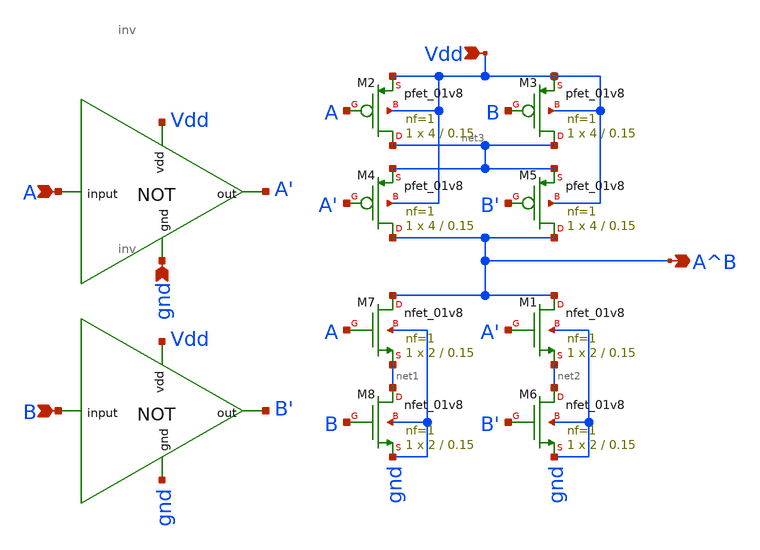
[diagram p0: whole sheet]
** sch_path: extra_stuff/xor.sch
**.subckt xor Vdd A B gnd A^B
*.ipin Vdd
*.ipin A
*.ipin B
*.ipin gnd
*.opin A^B
XM1 A^B A' net2 gnd sky130_fd_pr__nfet_01v8 L=0.15 W=2 nf=1 ad='int((1 + 1)/2) * 2 / 1 * 0.29' as='int((1
+ + 2)/2) * 2 / 1 * 0.29' pd='2*int((1 + 1)/2) * (2 / 1 + 0.29)' ps='2*int((1 + 2)/2) * (2 / 1 + 0.29)' nrd='0.29
+ / 2 ' nrs='0.29 / 2 ' sa=0 sb=0 sd=0 mult=1 m=1
XM2 net3 A Vdd Vdd sky130_fd_pr__pfet_01v8 L=0.15 W=4 nf=1 ad='int((1 + 1)/2) * 4 / 1 * 0.29' as='int((1
+ + 2)/2) * 4 / 1 * 0.29' pd='2*int((1 + 1)/2) * (4 / 1 + 0.29)' ps='2*int((1 + 2)/2) * (4 / 1 + 0.29)' nrd='0.29
+ / 4 ' nrs='0.29 / 4 ' sa=0 sb=0 sd=0 mult=1 m=1
XM3 net3 B Vdd Vdd sky130_fd_pr__pfet_01v8 L=0.15 W=4 nf=1 ad='int((1 + 1)/2) * 4 / 1 * 0.29' as='int((1
+ + 2)/2) * 4 / 1 * 0.29' pd='2*int((1 + 1)/2) * (4 / 1 + 0.29)' ps='2*int((1 + 2)/2) * (4 / 1 + 0.29)' nrd='0.29
+ / 4 ' nrs='0.29 / 4 ' sa=0 sb=0 sd=0 mult=1 m=1
XM4 A^B A' net3 Vdd sky130_fd_pr__pfet_01v8 L=0.15 W=4 nf=1 ad='int((1 + 1)/2) * 4 / 1 * 0.29' as='int((1 + 2)/2) * 4 / 1 * 0.29'
+ pd='2*int((1 + 1)/2) * (4 / 1 + 0.29)' ps='2*int((1 + 2)/2) * (4 / 1 + 0.29)' nrd='0.29 / 4 ' nrs='0.29 / 4 '
+ sa=0 sb=0 sd=0 mult=1 m=1
XM5 A^B B' net3 Vdd sky130_fd_pr__pfet_01v8 L=0.15 W=4 nf=1 ad='int((1 + 1)/2) * 4 / 1 * 0.29' as='int((1
+ + 2)/2) * 4 / 1 * 0.29' pd='2*int((1 + 1)/2) * (4 / 1 + 0.29)' ps='2*int((1 + 2)/2) * (4 / 1 + 0.29)' nrd='0.29
+ / 4 ' nrs='0.29 / 4 ' sa=0 sb=0 sd=0 mult=1 m=1
XM6 net2 B' gnd gnd sky130_fd_pr__nfet_01v8 L=0.15 W=2 nf=1 ad='int((1 + 1)/2) * 2 / 1 * 0.29' as='int((1 + 2)/2) * 2 / 1 * 0.29'
+ pd='2*int((1 + 1)/2) * (2 / 1 + 0.29)' ps='2*int((1 + 2)/2) * (2 / 1 + 0.29)' nrd='0.29 / 2 ' nrs='0.29 / 2 '
+ sa=0 sb=0 sd=0 mult=1 m=1
XM7 A^B A net1 gnd sky130_fd_pr__nfet_01v8 L=0.15 W=2 nf=1 ad='int((1 + 1)/2) * 2 / 1 * 0.29' as='int((1 + 2)/2) * 2 / 1 * 0.29'
+ pd='2*int((1 + 1)/2) * (2 / 1 + 0.29)' ps='2*int((1 + 2)/2) * (2 / 1 + 0.29)' nrd='0.29 / 2 ' nrs='0.29 / 2 '
+ sa=0 sb=0 sd=0 mult=1 m=1
XM8 net1 B gnd gnd sky130_fd_pr__nfet_01v8 L=0.15 W=2 nf=1 ad='int((1 + 1)/2) * 2 / 1 * 0.29' as='int((1 + 2)/2) * 2 / 1 * 0.29'
+ pd='2*int((1 + 1)/2) * (2 / 1 + 0.29)' ps='2*int((1 + 2)/2) * (2 / 1 + 0.29)' nrd='0.29 / 2 ' nrs='0.29 / 2 '
+ sa=0 sb=0 sd=0 mult=1 m=1
x1 A' Vdd A gnd inv
x2 B' Vdd B gnd inv
**.ends
.end
